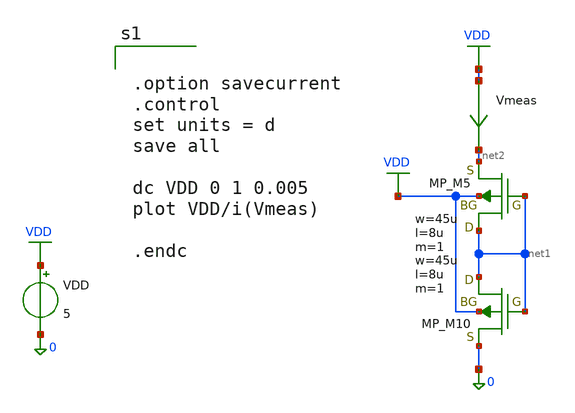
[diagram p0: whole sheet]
** sch_path: member_project/JJY_Receiver/Masahiro/jjy_recv/diff_amp/pseudo_res.sch
**.subckt pseudo_res
XM5 net1 net1 net2 VDD PMOS w=45u l=8u as=0 ad=0 ps=0 pd=0 nrd=0 nrs=0 m=1
XM10 net1 net1 0 VDD PMOS w=45u l=8u as=0 ad=0 ps=0 pd=0 nrd=0 nrs=0 m=1
Vmeas VDD net2 0
.save i(vmeas)
VDD VDD 0 5
**** begin user architecture code
 .include $::LIB/ip62_models


.option savecurrent
.control
set units = d
save all

dc VDD 0 1 0.005
plot VDD/i(Vmeas)

.endc


**** end user architecture code
**.ends
.GLOBAL VDD
.end
